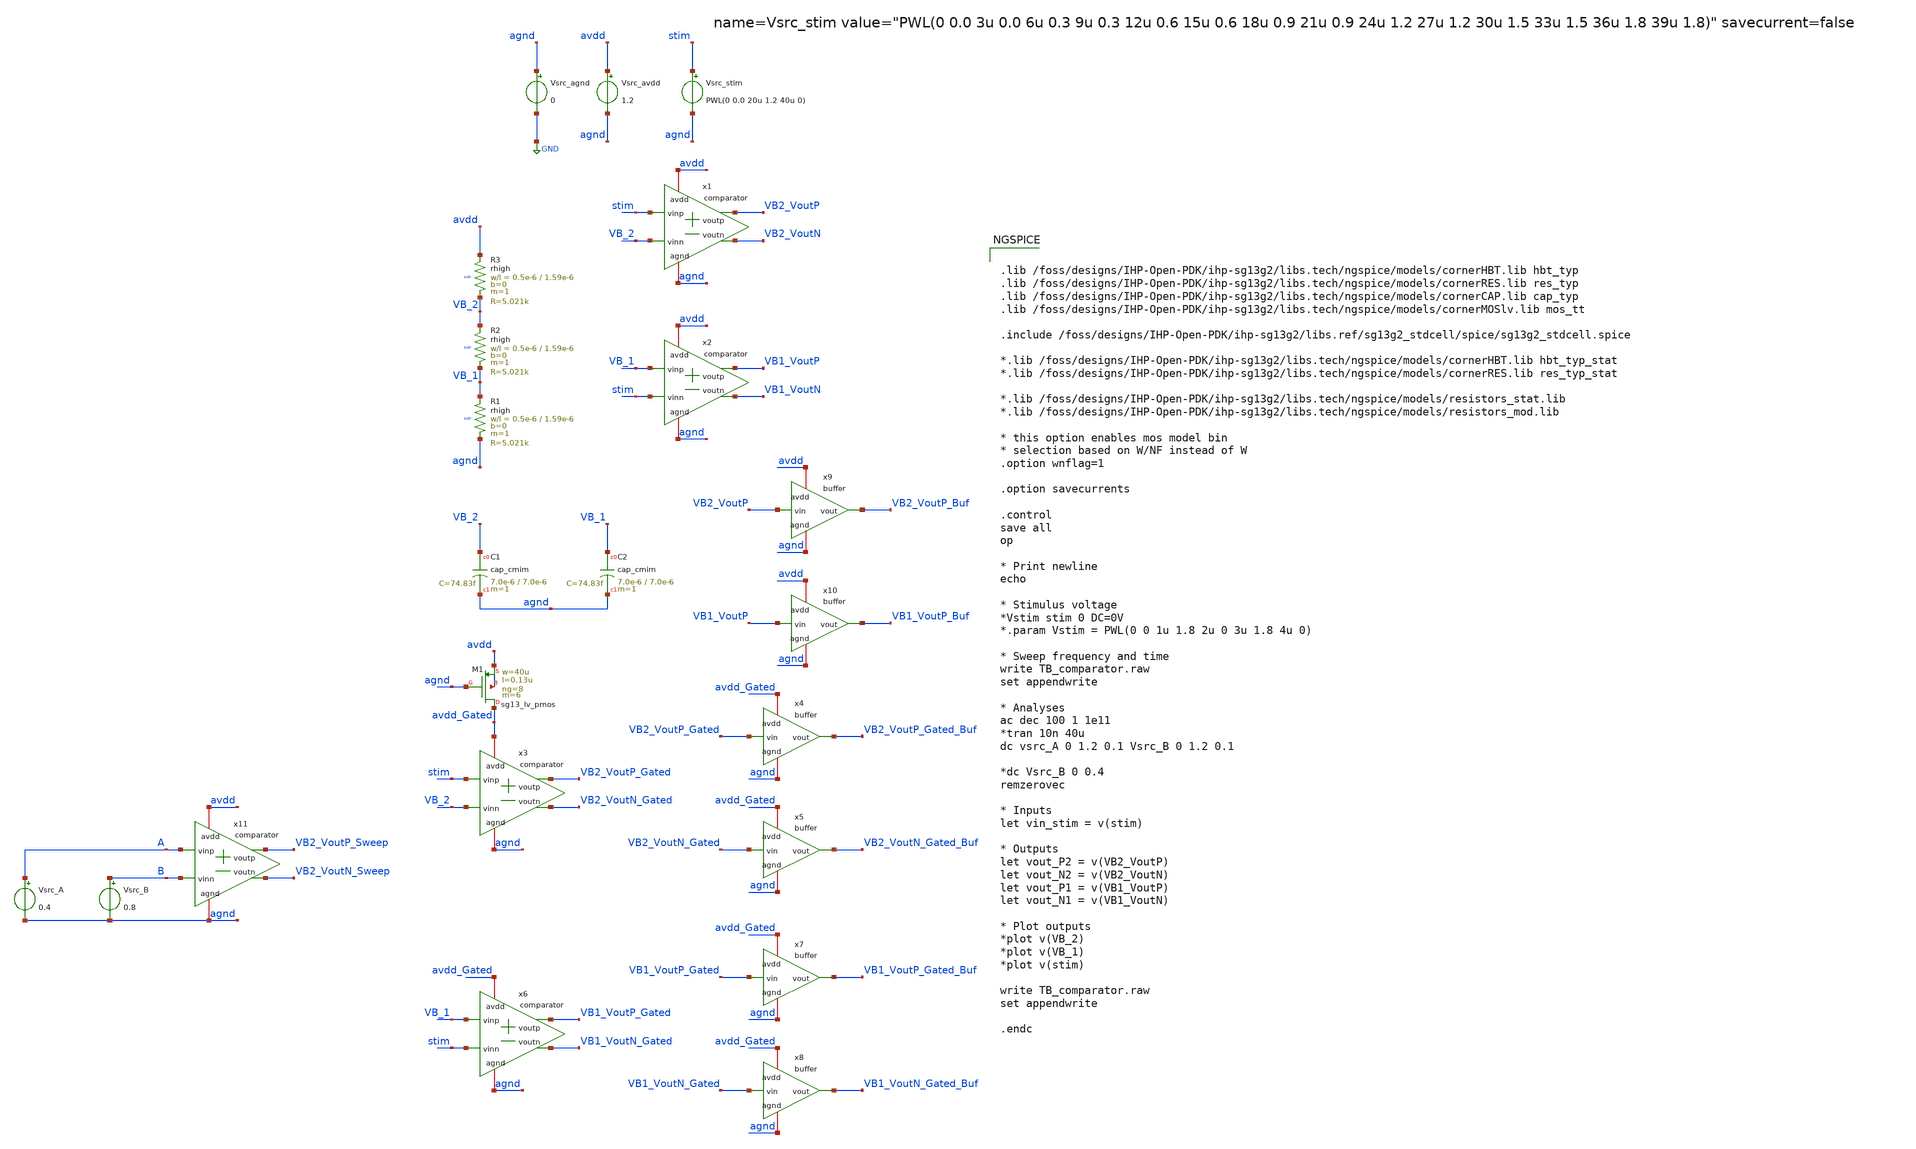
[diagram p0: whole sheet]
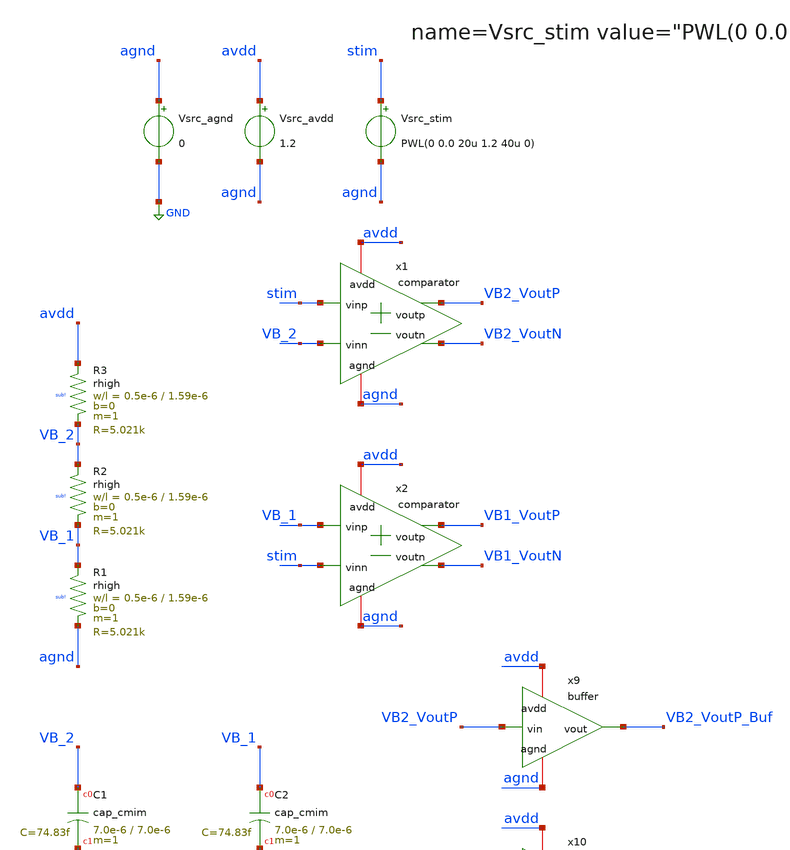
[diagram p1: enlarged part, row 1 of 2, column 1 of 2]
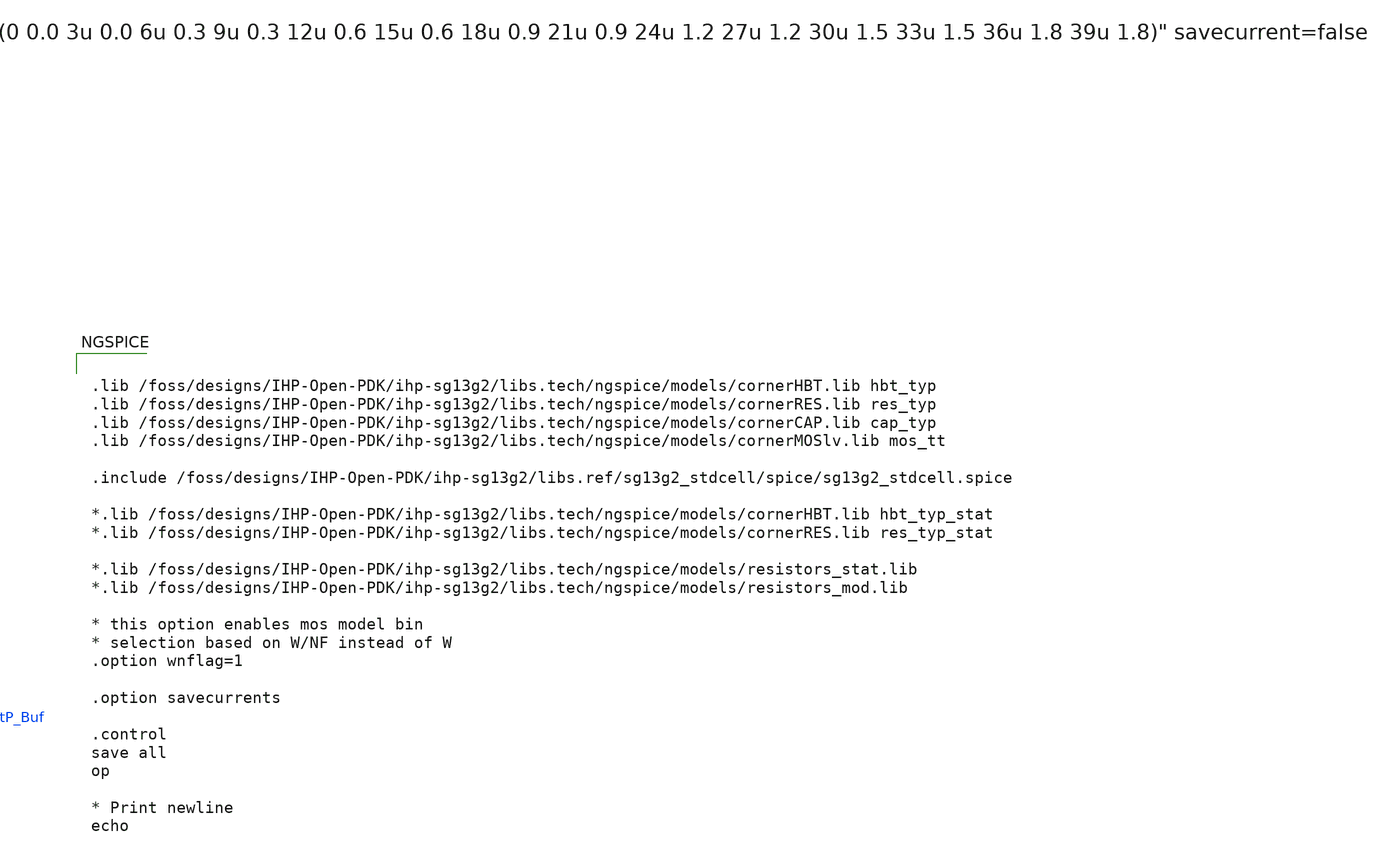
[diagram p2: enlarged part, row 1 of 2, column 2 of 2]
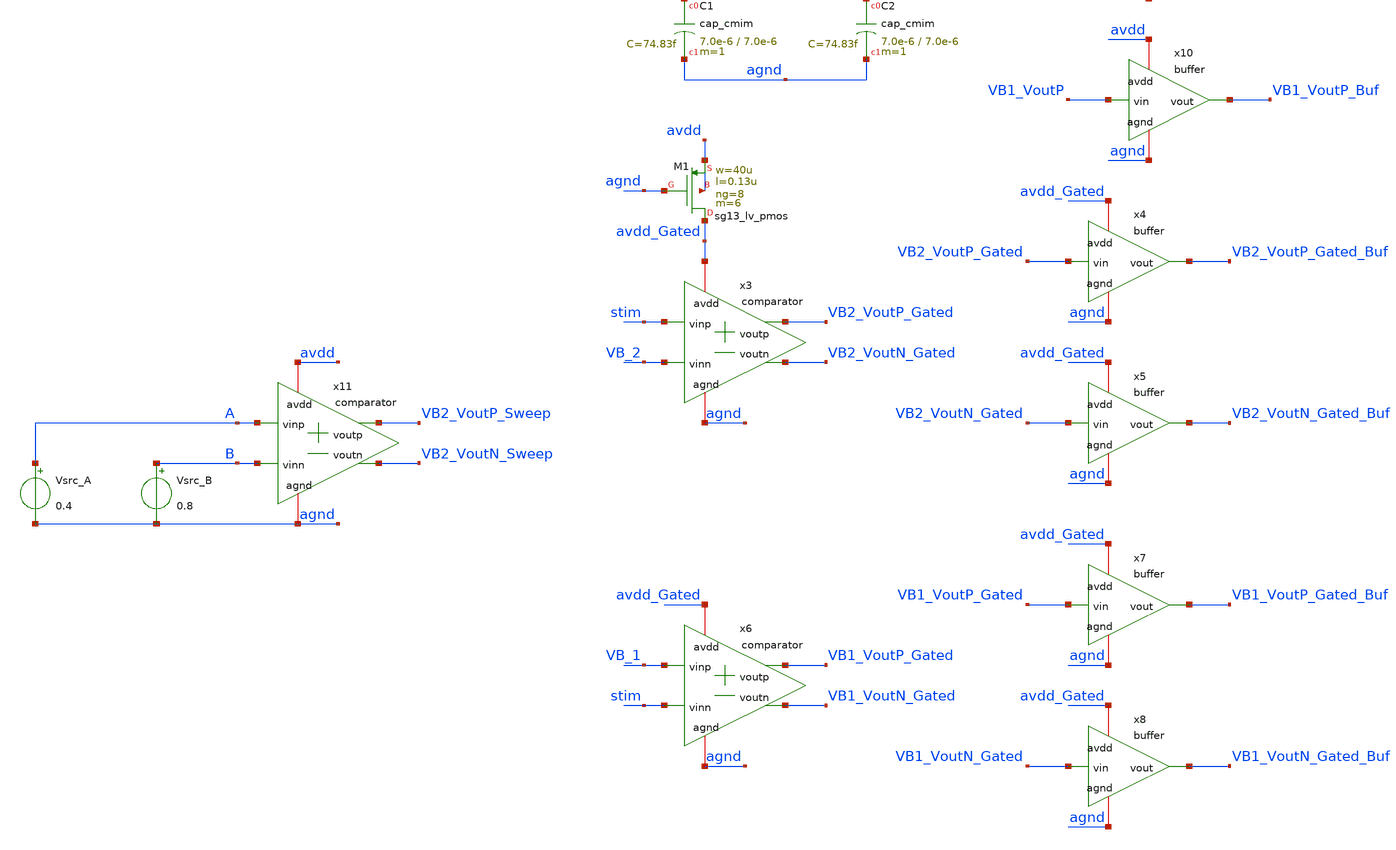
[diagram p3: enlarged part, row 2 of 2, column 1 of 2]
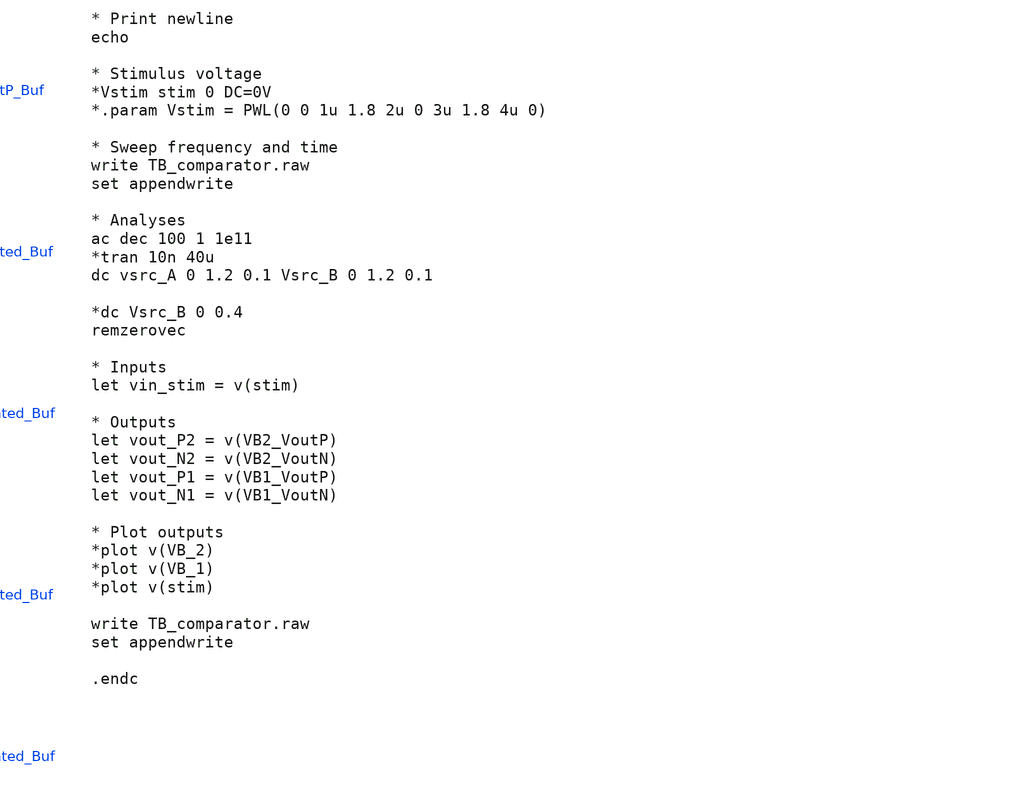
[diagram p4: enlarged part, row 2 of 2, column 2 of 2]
** sch_path: xschem/TB_comparator.sch
**.subckt TB_comparator
x1 avdd VB2_VoutP VB2_VoutN VB_2 stim agnd comparator
Vsrc_agnd agnd GND 0
Vsrc_avdd avdd agnd 1.2
x2 avdd VB1_VoutP VB1_VoutN stim VB_1 agnd comparator
XR3 avdd VB_2 sub! rhigh w=0.5e-6 l=1.59e-6 m=1 b=0 mm_ok=1
Vsrc_stim stim agnd PWL(0 0.0 20u 1.2 40u 0)
XR1 VB_1 agnd sub! rhigh w=0.5e-6 l=1.59e-6 m=1 b=0 mm_ok=1
XR2 VB_2 VB_1 sub! rhigh w=0.5e-6 l=1.59e-6 m=1 b=0 mm_ok=1
XC1 VB_2 agnd cap_cmim w=7.0e-6 l=7.0e-6 m=1 mm_ok=1
XC2 VB_1 agnd cap_cmim w=7.0e-6 l=7.0e-6 m=1 mm_ok=1
x9 avdd VB2_VoutP VB2_VoutP_Buf agnd buffer
x10 avdd VB1_VoutP VB1_VoutP_Buf agnd buffer
XM1 avdd_Gated agnd avdd avdd sg13_lv_pmos w=40u l=0.13u ng=8 m=6 mm_ok=1
x3 avdd_Gated VB2_VoutP_Gated VB2_VoutN_Gated VB_2 stim agnd comparator
x4 avdd_Gated VB2_VoutP_Gated VB2_VoutP_Gated_Buf agnd buffer
x5 avdd_Gated VB2_VoutN_Gated VB2_VoutN_Gated_Buf agnd buffer
x6 avdd_Gated VB1_VoutP_Gated VB1_VoutN_Gated stim VB_1 agnd comparator
x7 avdd_Gated VB1_VoutP_Gated VB1_VoutP_Gated_Buf agnd buffer
x8 avdd_Gated VB1_VoutN_Gated VB1_VoutN_Gated_Buf agnd buffer
x11 avdd VB2_VoutP_Sweep VB2_VoutN_Sweep B A agnd comparator
Vsrc_B B agnd 0.8
Vsrc_A A agnd 0.4
**** begin user architecture code


.lib /foss/designs/IHP-Open-PDK/ihp-sg13g2/libs.tech/ngspice/models/cornerHBT.lib hbt_typ
.lib /foss/designs/IHP-Open-PDK/ihp-sg13g2/libs.tech/ngspice/models/cornerRES.lib res_typ
.lib /foss/designs/IHP-Open-PDK/ihp-sg13g2/libs.tech/ngspice/models/cornerCAP.lib cap_typ
.lib /foss/designs/IHP-Open-PDK/ihp-sg13g2/libs.tech/ngspice/models/cornerMOSlv.lib mos_tt

.include /foss/designs/IHP-Open-PDK/ihp-sg13g2/libs.ref/sg13g2_stdcell/spice/sg13g2_stdcell.spice

*.lib /foss/designs/IHP-Open-PDK/ihp-sg13g2/libs.tech/ngspice/models/cornerHBT.lib hbt_typ_stat
*.lib /foss/designs/IHP-Open-PDK/ihp-sg13g2/libs.tech/ngspice/models/cornerRES.lib res_typ_stat

*.lib /foss/designs/IHP-Open-PDK/ihp-sg13g2/libs.tech/ngspice/models/resistors_stat.lib
*.lib /foss/designs/IHP-Open-PDK/ihp-sg13g2/libs.tech/ngspice/models/resistors_mod.lib

* this option enables mos model bin
* selection based on W/NF instead of W
.option wnflag=1

.option savecurrents

.control
save all
op

* Print newline
echo

* Stimulus voltage
*Vstim stim 0 DC=0V
*.param Vstim = PWL(0 0 1u 1.8 2u 0 3u 1.8 4u 0)

* Sweep frequency and time
write TB_comparator.raw
set appendwrite

* Analyses
ac dec 100 1 1e11
*tran 10n 40u
dc vsrc_A 0 1.2 0.1 Vsrc_B 0 1.2 0.1

*dc Vsrc_B 0 0.4
remzerovec

* Inputs
let vin_stim = v(stim)

* Outputs
let vout_P2 = v(VB2_VoutP)
let vout_N2 = v(VB2_VoutN)
let vout_P1 = v(VB1_VoutP)
let vout_N1 = v(VB1_VoutN)

* Plot outputs
*plot v(VB_2)
*plot v(VB_1)
*plot v(stim)

write TB_comparator.raw
set appendwrite

.endc


**** end user architecture code
**.ends

* expanding   symbol:  comparator.sym # of pins=6
** sym_path: xschem/comparator.sym
** sch_path: xschem/comparator.sch
.subckt comparator avdd voutp voutn vinn vinp agnd
*.iopin avdd
*.ipin vinp
*.opin voutp
*.iopin agnd
*.ipin vinn
*.opin voutn
XQ1 voutp vinn ee agnd npn13G2 Nx=1 mm_ok=1
XR1 avdd voutp sub! rppd w=0.5e-6 l=20e-6 m=1 b=0 mm_ok=1
XR2 ee agnd sub! rppd w=0.5e-6 l=2e-6 m=1 b=0 mm_ok=1
XR3 avdd voutn sub! rppd w=0.5e-6 l=20e-6 m=1 b=0 mm_ok=1
XQ2 voutn vinp ee agnd npn13G2 Nx=1 mm_ok=1
.ends


* expanding   symbol:  buffer.sym # of pins=4
** sym_path: xschem/buffer.sym
** sch_path: xschem/buffer.sch
.subckt buffer avdd vin vout agnd
*.iopin avdd
*.ipin vin
*.opin vout
*.iopin agnd
x1 avdd vin net1 agnd inverter
x2 avdd net1 vout agnd inverter
.ends


* expanding   symbol:  inverter.sym # of pins=4
** sym_path: xschem/inverter.sym
** sch_path: xschem/inverter.sch
.subckt inverter avdd vin vout agnd
*.iopin avdd
*.ipin vin
*.opin vout
*.iopin agnd
XQ1 vout base agnd agnd npn13G2 Nx=10 mm_ok=1
XR1 avdd vout sub! rhigh w=1e-6 l=0.5e-6 m=1 b=0 mm_ok=1
XR2 base vin sub! rhigh w=0.5e-6 l=0.5e-6 m=1 b=0 mm_ok=1
.ends

.GLOBAL GND
.end
